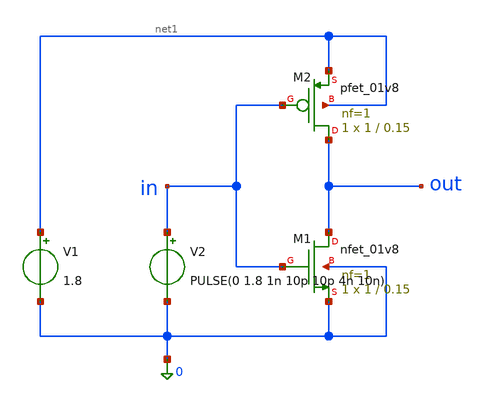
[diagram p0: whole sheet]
** sch_path: xsch/inverter.sch
**.subckt inverter
XM1 out in 0 0 sky130_fd_pr__nfet_01v8 L=0.15 W=1 nf=1 ad='int((1 + 1)/2) * 1 / 1 * 0.29' as='int((1 + 2)/2) * 1 / 1 * 0.29'
+ pd='2*int((1 + 1)/2) * (1 / 1 + 0.29)' ps='2*int((1 + 2)/2) * (1 / 1 + 0.29)' nrd='0.29 / 1 ' nrs='0.29 / 1 '
+ sa=0 sb=0 sd=0 mult=1 m=1
XM2 out in net1 net1 sky130_fd_pr__pfet_01v8 L=0.15 W=1 nf=1 ad='int((1 + 1)/2) * 1 / 1 * 0.29' as='int((1 + 2)/2) * 1 / 1 * 0.29'
+ pd='2*int((1 + 1)/2) * (1 / 1 + 0.29)' ps='2*int((1 + 2)/2) * (1 / 1 + 0.29)' nrd='0.29 / 1 ' nrs='0.29 / 1 '
+ sa=0 sb=0 sd=0 mult=1 m=1
V1 net1 0 1.8
V2 in 0 PULSE(0 1.8 1n 10p 10p 4n 10n)
**** begin user architecture code
 .lib /foss/pdks/sky130A/libs.tech/ngspice/sky130.lib.spice tt

.param mc_mm_switch=0
.param mc_pr_switch=1



.option wnflag=0
.option savecurrents
.control
save all
*dc v2 0 1.8 0.01
tran 10ps 10ns
plot in out
op
.endc


**** end user architecture code
**.ends
.end
